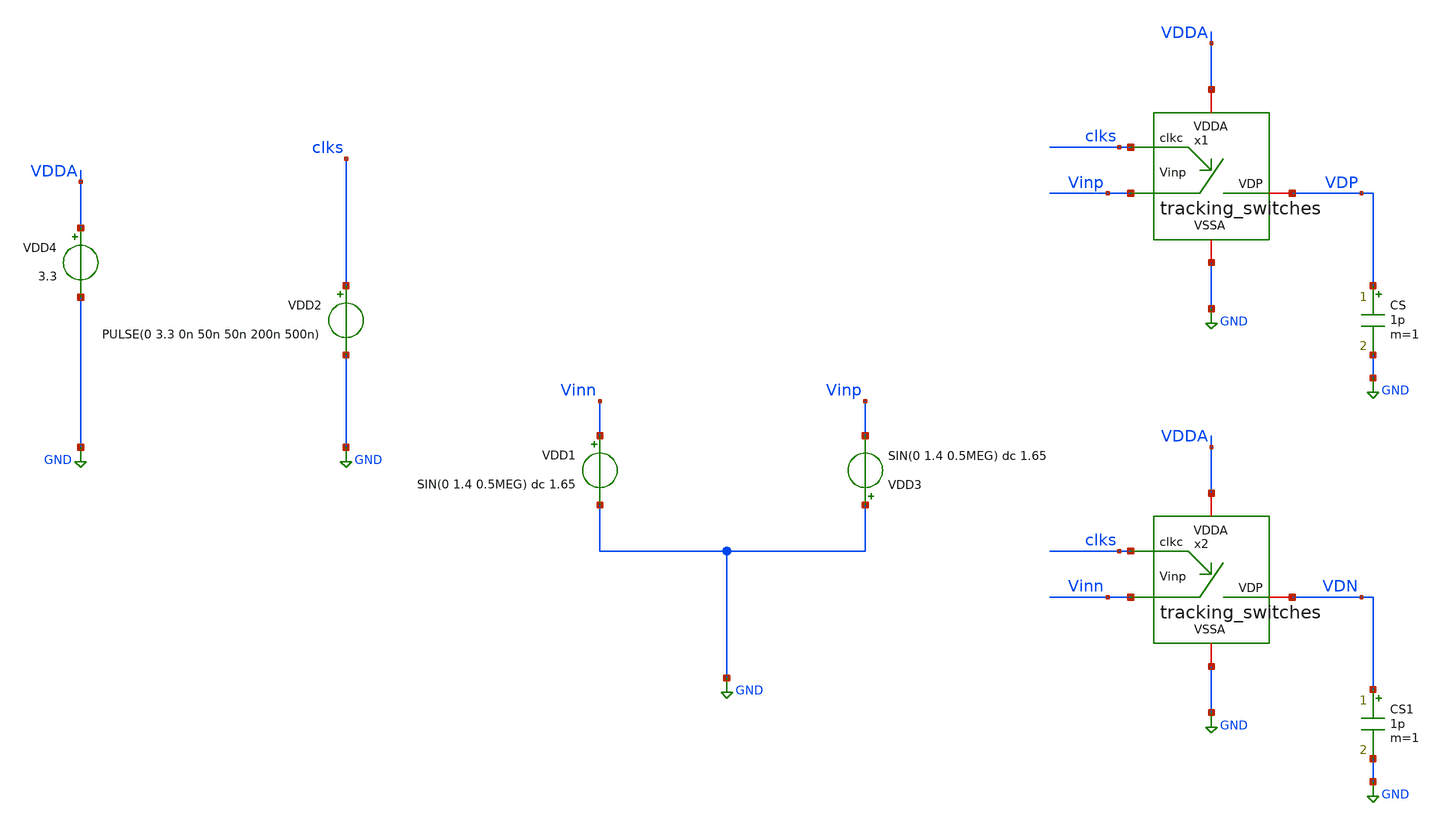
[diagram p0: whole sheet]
** sch_path: SAR_ADC/blocks/tracking_switches/tracking_switches_tb.sch
**.subckt tracking_switches_tb
x1 VDP VDDA GND clks Vinp tracking_switches
VDD2 clks GND PULSE(0 3.3 0n 50n 50n 200n 500n)
VDD4 VDDA GND 3.3
CS VDP GND 1p m=1
x2 VDN VDDA GND clks Vinn tracking_switches
CS1 VDN GND 1p m=1
VDD1 Vinn GND SIN(0 1.4 0.5MEG) dc 1.65
VDD3 GND Vinp SIN(0 1.4 0.5MEG) dc 1.65
**** begin user architecture code



*Parameters

.options TEMP = 50.0
.lib /home/electrica/Documents/gf180_projects/pdk/gf180mcuC/libs.tech/ngspice/sm141064.ngspice typical
.include /home/electrica/Documents/gf180_projects/pdk/gf180mcuC/libs.tech/ngspice/design.ngspice

*Data to save
.save all


* Simulation
.control
tran 0.1n 5u 0.01n
*setplot dc1
*let Vgs_xm1 = V(.x1.VG_XM1) - V(.x1.VS_XM1)
*let Vds_xm1 = V(.x1.VS_XM1) - V(Vinp)
*plot Vgs_xm1 Vds_xm1

*setplot dc2
*let Vgs_xm2 = V(.x1.n_clkc)
*let Vds_xm2 = V(.x1.VS_XM1)
*plot Vgs_xm2 Vds_xm2

*setplot dc3
*let Vgs_xm3 = V(.x1.VG_XM1) - V(.x1.VS_XM1)
*let Vds_xm3 = V(.x1.VD_XM5) - V(.x1.VS_XM1)
*plot Vgs_xm3 Vds_xm3

*setplot dc4
*let Vgs_xm4 = V(clkc) - V(.x1.VS_XM1)
*let Vds_xm4 = V(.x1.VD_XM5) - V(.x1.VS_XM1)
*plot Vgs_xm4 Vds_xm4

*setplot dc5
*let Vsg_xm5 = V(VDDA) - V(clkc)
*let vsd_xm5 = V(.x1.VD_XM5)
*plot Vsg_xm5 vsd_xm5

*setplot dc6
*let Vsg_xm6 = V(VDDA) - V(.x1.VG_XM1)
*let vsd_xm6 = V(VDDA) - V(.x1.VS_XM6)
*plot Vsg_xm6 vsd_xm6

*setplot dc7
*let Vsg_xm7 = V(.x1.VS_XM6) - V(.x1.VD_XM5)
*let vsd_xm7 = V(.x1.VS_XM6) - V(.x1.VG_XM1)
*plot Vsg_xm7 vsd_xm7

*setplot dc8
*let Vsg_xm8 = V(VDDA) - V(.x1.VS_XM8)
*let vsd_xm8 = V(.x1.VG_XM1) - V(.x1.VS_XM8)
*plot Vsg_xm8 vsd_xm8

*setplot dc9
*let Vsg_xm9 = V(.x1.n_clkc)
*let vsd_xm9 = V(.x1.VS_XM8)
*plot Vsg_xm9 vsd_xm9

setplot dc10
plot V(clks)+20 V(Vinp)+16 V(Vinn)+12 V(VDP)+4 V(VDN)
set filetype = ascii
write tracking_switches_tb_tran.raw

reset
unset filetype
op
save all
write tracking_switches_tb.raw


.endc
.end


**** end user architecture code
**.ends

* expanding   symbol:
*+  /home/electrica/Documents/gf180_projects/gf180_work/PICO_contest/tracking_switches/tracking_switches.sym # of pins=5
** sym_path: SAR_ADC/blocks/tracking_switches/tracking_switches.sym
** sch_path: SAR_ADC/blocks/tracking_switches/tracking_switches.sch
.subckt tracking_switches VDP VDDA VSSA clkc Vinp
*.iopin VDDA
*.iopin VSSA
*.ipin clkc
*.ipin Vinp
*.iopin VDP
XM2 VS_XM1 n_clkc VSSA VSSA nfet_03v3 L=0.28u W=0.28u nf=1 ad='int((nf+1)/2) * W/nf * 0.18u' as='int((nf+2)/2) * W/nf * 0.18u'
+ pd='2*int((nf+1)/2) * (W/nf + 0.18u)' ps='2*int((nf+2)/2) * (W/nf + 0.18u)' nrd='0.18u / W' nrs='0.18u / W'
+ sa=0 sb=0 sd=0 m=1
XM4 VD_XM5 clkc VS_XM1 VSSA nfet_03v3 L=0.28u W=0.28u nf=1 ad='int((nf+1)/2) * W/nf * 0.18u' as='int((nf+2)/2) * W/nf * 0.18u'
+ pd='2*int((nf+1)/2) * (W/nf + 0.18u)' ps='2*int((nf+2)/2) * (W/nf + 0.18u)' nrd='0.18u / W' nrs='0.18u / W'
+ sa=0 sb=0 sd=0 m=1
XM3 VD_XM5 VG_XM1 VS_XM1 VSSA nfet_03v3 L=0.28u W=0.28u nf=1 ad='int((nf+1)/2) * W/nf * 0.18u' as='int((nf+2)/2) * W/nf * 0.18u'
+ pd='2*int((nf+1)/2) * (W/nf + 0.18u)' ps='2*int((nf+2)/2) * (W/nf + 0.18u)' nrd='0.18u / W' nrs='0.18u / W'
+ sa=0 sb=0 sd=0 m=1
XM5 VD_XM5 clkc VDDA VDDA pfet_03v3 L=0.28u W=0.28u nf=1 ad='int((nf+1)/2) * W/nf * 0.18u' as='int((nf+2)/2) * W/nf * 0.18u'
+ pd='2*int((nf+1)/2) * (W/nf + 0.18u)' ps='2*int((nf+2)/2) * (W/nf + 0.18u)' nrd='0.18u / W' nrs='0.18u / W'
+ sa=0 sb=0 sd=0 m=3
XM6 VDDA VG_XM1 VS_XM6 VS_XM6 pfet_03v3 L=0.28u W=0.28u nf=1 ad='int((nf+1)/2) * W/nf * 0.18u' as='int((nf+2)/2) * W/nf * 0.18u'
+ pd='2*int((nf+1)/2) * (W/nf + 0.18u)' ps='2*int((nf+2)/2) * (W/nf + 0.18u)' nrd='0.18u / W' nrs='0.18u / W'
+ sa=0 sb=0 sd=0 m=3
CB VS_XM6 VS_XM1 1p m=1
XM7 VG_XM1 VD_XM5 VS_XM6 VS_XM6 pfet_03v3 L=0.28u W=0.28u nf=1 ad='int((nf+1)/2) * W/nf * 0.18u' as='int((nf+2)/2) * W/nf * 0.18u'
+ pd='2*int((nf+1)/2) * (W/nf + 0.18u)' ps='2*int((nf+2)/2) * (W/nf + 0.18u)' nrd='0.18u / W' nrs='0.18u / W'
+ sa=0 sb=0 sd=0 m=1
XM1 Vinp VG_XM1 VS_XM1 VSSA nfet_03v3 L=0.28u W=0.28u nf=1 ad='int((nf+1)/2) * W/nf * 0.18u' as='int((nf+2)/2) * W/nf * 0.18u'
+ pd='2*int((nf+1)/2) * (W/nf + 0.18u)' ps='2*int((nf+2)/2) * (W/nf + 0.18u)' nrd='0.18u / W' nrs='0.18u / W'
+ sa=0 sb=0 sd=0 m=1
XM9 VS_XM8 n_clkc VSSA VSSA nfet_03v3 L=0.28u W=0.28u nf=1 ad='int((nf+1)/2) * W/nf * 0.18u' as='int((nf+2)/2) * W/nf * 0.18u'
+ pd='2*int((nf+1)/2) * (W/nf + 0.18u)' ps='2*int((nf+2)/2) * (W/nf + 0.18u)' nrd='0.18u / W' nrs='0.18u / W'
+ sa=0 sb=0 sd=0 m=1
XM8 VG_XM1 VDDA VS_XM8 VSSA nfet_03v3 L=0.28u W=0.28u nf=1 ad='int((nf+1)/2) * W/nf * 0.18u' as='int((nf+2)/2) * W/nf * 0.18u'
+ pd='2*int((nf+1)/2) * (W/nf + 0.18u)' ps='2*int((nf+2)/2) * (W/nf + 0.18u)' nrd='0.18u / W' nrs='0.18u / W'
+ sa=0 sb=0 sd=0 m=1
XMS VDP VG_XM1 Vinp VSSA nfet_03v3 L=0.28u W=0.28u nf=1 ad='int((nf+1)/2) * W/nf * 0.18u' as='int((nf+2)/2) * W/nf * 0.18u'
+ pd='2*int((nf+1)/2) * (W/nf + 0.18u)' ps='2*int((nf+2)/2) * (W/nf + 0.18u)' nrd='0.18u / W' nrs='0.18u / W'
+ sa=0 sb=0 sd=0 m=1
x1 VDDA VSSA n_clkc clkc tracking_switches_inv_1x
.ends


* expanding   symbol:
*+  /home/electrica/Documents/gf180_projects/gf180_work/PICO_contest/tracking_switches/tracking_switches_inv_1x.sym # of pins=4
** sym_path: SAR_ADC/blocks/tracking_switches/tracking_switches_inv_1x.sym
** sch_path: SAR_ADC/blocks/tracking_switches/tracking_switches_inv_1x.sch
.subckt tracking_switches_inv_1x VDDA VSSA OUT IN
*.iopin VDDA
*.iopin VSSA
*.iopin OUT
*.ipin IN
XM1 OUT IN VSSA VSSA nfet_03v3 L=0.28u W=0.22u nf=1 ad='int((nf+1)/2) * W/nf * 0.18u' as='int((nf+2)/2) * W/nf * 0.18u'
+ pd='2*int((nf+1)/2) * (W/nf + 0.18u)' ps='2*int((nf+2)/2) * (W/nf + 0.18u)' nrd='0.18u / W' nrs='0.18u / W'
+ sa=0 sb=0 sd=0 m=1
XM2 OUT IN VDDA VDDA pfet_03v3 L=0.28u W=0.66u nf=1 ad='int((nf+1)/2) * W/nf * 0.18u' as='int((nf+2)/2) * W/nf * 0.18u'
+ pd='2*int((nf+1)/2) * (W/nf + 0.18u)' ps='2*int((nf+2)/2) * (W/nf + 0.18u)' nrd='0.18u / W' nrs='0.18u / W'
+ sa=0 sb=0 sd=0 m=1
.ends

.GLOBAL GND
.end
